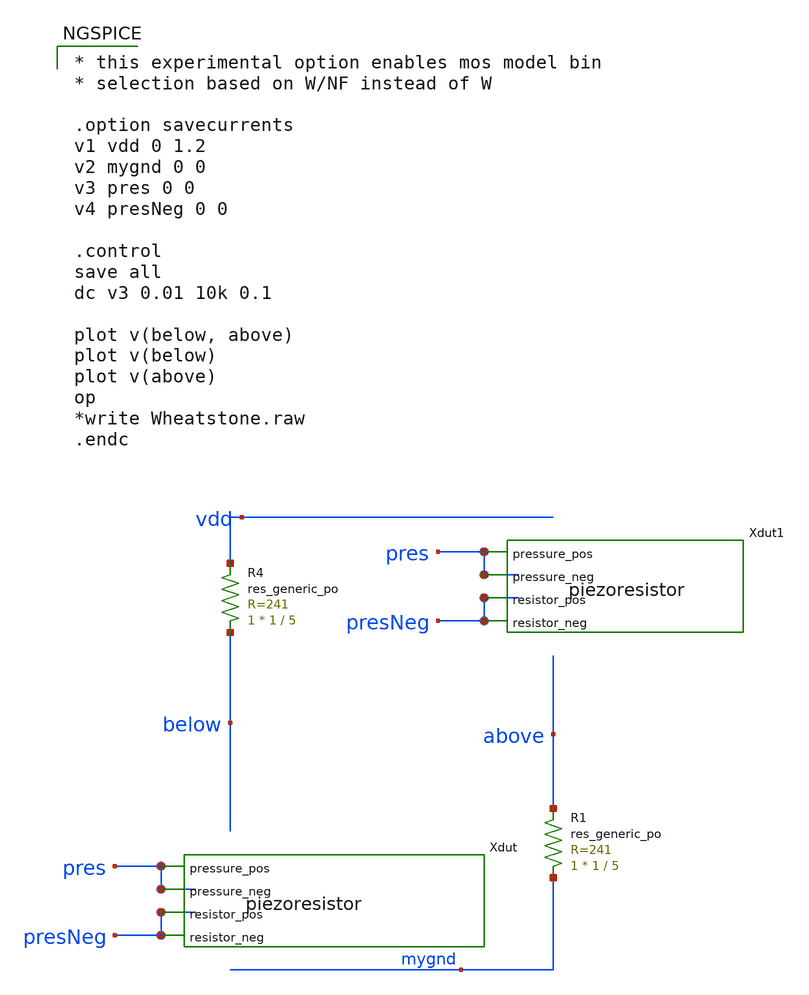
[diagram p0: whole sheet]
** sch_path: circuits/Wheatstone.sch
* Copyright 2020 Stefan Frederik Schippers
* Licensed under the Apache License, Version 2.0 (the "License");
* you may not use this file except in compliance with the License.
* You may obtain a copy of the License at
* https://www.apache.org/licenses/LICENSE-2.0
* Unless required by applicable law or agreed to in writing, software
* distributed under the License is distributed on an "AS IS" BASIS,
* WITHOUT WARRANTIES OR CONDITIONS OF ANY KIND, either express or implied.
* See the License for the specific language governing permissions and
* limitations under the License.
**.subckt Wheatstone
Xdut pres pres presNeg presNeg piezoresistor
Xdut1 pres pres presNeg presNeg piezoresistor
XR4 below vdd sky130_fd_pr__res_generic_po W=1 L=5 m=1
XR1 mygnd above sky130_fd_pr__res_generic_po W=1 L=5 m=1
**** begin user architecture code
 .lib $::SKYWATER_MODELS/models/sky130.lib.spice tt

.param mc_mm_switch=0
.param mc_pr_switch=1



* this experimental option enables mos model bin
* selection based on W/NF instead of W

.option savecurrents
v1 vdd 0 1.2
v2 mygnd 0 0
v3 pres 0 0
v4 presNeg 0 0

.control
save all
dc v3 0.01 10k 0.1

plot v(below, above)
plot v(below)
plot v(above)
op
*write Wheatstone.raw
.endc


**** end user architecture code
**.ends

* expanding   symbol:  piezoresistor.sym # of pins=4
** sym_path: circuits/piezoresistor.sym
** sch_path: circuits/piezoresistor.sch
.subckt piezoresistor pressure_pos pressure_neg resistor_pos resistor_neg
*.ipin pressure_pos
*.ipin pressure_neg
*.iopin resistor_pos
*.iopin resistor_neg
Broot sqrtp 0 V = sqrt(v(pressure_pos,pressure_neg))
Bres res 0 V = 106*(50/v(sqrtp)-1)*exp(-0.328*v(sqrtp))+15
Brvar resistor_pos resistor_neg I = V(resistor_pos,resistor_neg)/V(res)
.ends

.end
